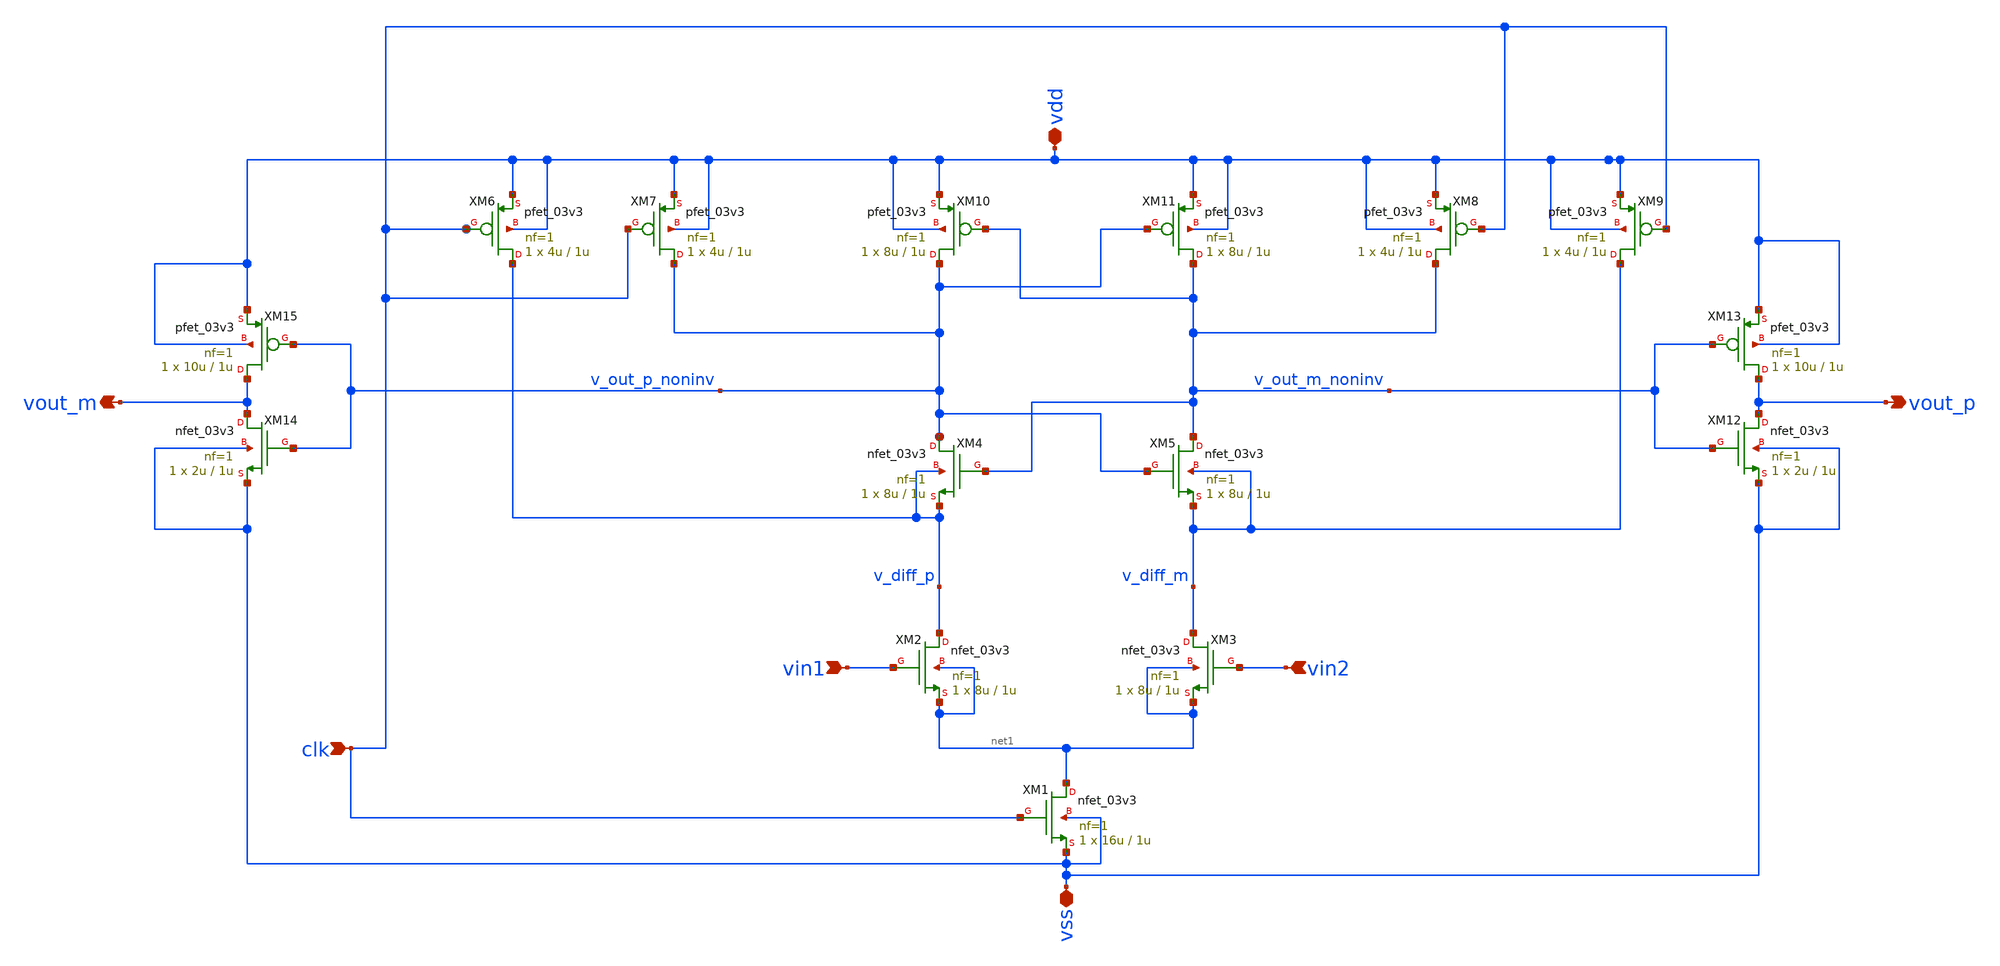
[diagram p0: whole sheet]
** sch_path: Felix/Comparator.sch
**.subckt Comparator vdd vss clk vin1 vin2 vout_p vout_m
*.iopin vdd
*.iopin vss
*.ipin clk
*.ipin vin1
*.ipin vin2
*.opin vout_p
*.opin vout_m
XM1 net1 clk vss vss nfet_03v3 L=1u W=16u nf=1 ad='int((nf+1)/2) * W/nf * 0.18u' as='int((nf+2)/2) * W/nf * 0.18u'
+ pd='2*int((nf+1)/2) * (W/nf + 0.18u)' ps='2*int((nf+2)/2) * (W/nf + 0.18u)' nrd='0.18u / W' nrs='0.18u / W'
+ sa=0 sb=0 sd=0 m=1
XM2 v_diff_p vin1 net1 net1 nfet_03v3 L=1u W=8u nf=1 ad='int((nf+1)/2) * W/nf * 0.18u' as='int((nf+2)/2) * W/nf * 0.18u'
+ pd='2*int((nf+1)/2) * (W/nf + 0.18u)' ps='2*int((nf+2)/2) * (W/nf + 0.18u)' nrd='0.18u / W' nrs='0.18u / W'
+ sa=0 sb=0 sd=0 m=1
XM3 v_diff_m vin2 net1 net1 nfet_03v3 L=1u W=8u nf=1 ad='int((nf+1)/2) * W/nf * 0.18u' as='int((nf+2)/2) * W/nf * 0.18u'
+ pd='2*int((nf+1)/2) * (W/nf + 0.18u)' ps='2*int((nf+2)/2) * (W/nf + 0.18u)' nrd='0.18u / W' nrs='0.18u / W'
+ sa=0 sb=0 sd=0 m=1
XM4 v_out_p_noninv v_out_m_noninv v_diff_p v_diff_p nfet_03v3 L=1u W=8u nf=1 ad='int((nf+1)/2) * W/nf * 0.18u'
+ as='int((nf+2)/2) * W/nf * 0.18u' pd='2*int((nf+1)/2) * (W/nf + 0.18u)' ps='2*int((nf+2)/2) * (W/nf + 0.18u)'
+ nrd='0.18u / W' nrs='0.18u / W' sa=0 sb=0 sd=0 m=1
XM5 v_out_m_noninv v_out_p_noninv v_diff_m v_diff_m nfet_03v3 L=1u W=8u nf=1 ad='int((nf+1)/2) * W/nf * 0.18u'
+ as='int((nf+2)/2) * W/nf * 0.18u' pd='2*int((nf+1)/2) * (W/nf + 0.18u)' ps='2*int((nf+2)/2) * (W/nf + 0.18u)'
+ nrd='0.18u / W' nrs='0.18u / W' sa=0 sb=0 sd=0 m=1
XM6 v_diff_p clk vdd vdd pfet_03v3 L=1u W=4u nf=1 ad='int((nf+1)/2) * W/nf * 0.18u' as='int((nf+2)/2) * W/nf * 0.18u'
+ pd='2*int((nf+1)/2) * (W/nf + 0.18u)' ps='2*int((nf+2)/2) * (W/nf + 0.18u)' nrd='0.18u / W' nrs='0.18u / W'
+ sa=0 sb=0 sd=0 m=1
XM7 v_out_p_noninv clk vdd vdd pfet_03v3 L=1u W=4u nf=1 ad='int((nf+1)/2) * W/nf * 0.18u' as='int((nf+2)/2) * W/nf * 0.18u'
+ pd='2*int((nf+1)/2) * (W/nf + 0.18u)' ps='2*int((nf+2)/2) * (W/nf + 0.18u)' nrd='0.18u / W' nrs='0.18u / W'
+ sa=0 sb=0 sd=0 m=1
XM8 v_out_m_noninv clk vdd vdd pfet_03v3 L=1u W=4u nf=1 ad='int((nf+1)/2) * W/nf * 0.18u' as='int((nf+2)/2) * W/nf * 0.18u'
+ pd='2*int((nf+1)/2) * (W/nf + 0.18u)' ps='2*int((nf+2)/2) * (W/nf + 0.18u)' nrd='0.18u / W' nrs='0.18u / W'
+ sa=0 sb=0 sd=0 m=1
XM9 v_diff_m clk vdd vdd pfet_03v3 L=1u W=4u nf=1 ad='int((nf+1)/2) * W/nf * 0.18u' as='int((nf+2)/2) * W/nf * 0.18u'
+ pd='2*int((nf+1)/2) * (W/nf + 0.18u)' ps='2*int((nf+2)/2) * (W/nf + 0.18u)' nrd='0.18u / W' nrs='0.18u / W'
+ sa=0 sb=0 sd=0 m=1
XM10 v_out_p_noninv v_out_m_noninv vdd vdd pfet_03v3 L=1u W=8u nf=1 ad='int((nf+1)/2) * W/nf * 0.18u'
+ as='int((nf+2)/2) * W/nf * 0.18u' pd='2*int((nf+1)/2) * (W/nf + 0.18u)' ps='2*int((nf+2)/2) * (W/nf + 0.18u)'
+ nrd='0.18u / W' nrs='0.18u / W' sa=0 sb=0 sd=0 m=1
XM11 v_out_m_noninv v_out_p_noninv vdd vdd pfet_03v3 L=1u W=8u nf=1 ad='int((nf+1)/2) * W/nf * 0.18u'
+ as='int((nf+2)/2) * W/nf * 0.18u' pd='2*int((nf+1)/2) * (W/nf + 0.18u)' ps='2*int((nf+2)/2) * (W/nf + 0.18u)'
+ nrd='0.18u / W' nrs='0.18u / W' sa=0 sb=0 sd=0 m=1
XM12 vout_p v_out_m_noninv vss vss nfet_03v3 L=1u W=2u nf=1 ad='int((nf+1)/2) * W/nf * 0.18u' as='int((nf+2)/2) * W/nf * 0.18u'
+ pd='2*int((nf+1)/2) * (W/nf + 0.18u)' ps='2*int((nf+2)/2) * (W/nf + 0.18u)' nrd='0.18u / W' nrs='0.18u / W'
+ sa=0 sb=0 sd=0 m=1
XM13 vout_p v_out_m_noninv vdd vdd pfet_03v3 L=1u W=10u nf=1 ad='int((nf+1)/2) * W/nf * 0.18u' as='int((nf+2)/2) * W/nf * 0.18u'
+ pd='2*int((nf+1)/2) * (W/nf + 0.18u)' ps='2*int((nf+2)/2) * (W/nf + 0.18u)' nrd='0.18u / W' nrs='0.18u / W'
+ sa=0 sb=0 sd=0 m=1
XM14 vout_m v_out_p_noninv vss vss nfet_03v3 L=1u W=2u nf=1 ad='int((nf+1)/2) * W/nf * 0.18u' as='int((nf+2)/2) * W/nf * 0.18u'
+ pd='2*int((nf+1)/2) * (W/nf + 0.18u)' ps='2*int((nf+2)/2) * (W/nf + 0.18u)' nrd='0.18u / W' nrs='0.18u / W'
+ sa=0 sb=0 sd=0 m=1
XM15 vout_m v_out_p_noninv vdd vdd pfet_03v3 L=1u W=10u nf=1 ad='int((nf+1)/2) * W/nf * 0.18u' as='int((nf+2)/2) * W/nf * 0.18u'
+ pd='2*int((nf+1)/2) * (W/nf + 0.18u)' ps='2*int((nf+2)/2) * (W/nf + 0.18u)' nrd='0.18u / W' nrs='0.18u / W'
+ sa=0 sb=0 sd=0 m=1
**.ends
.end
